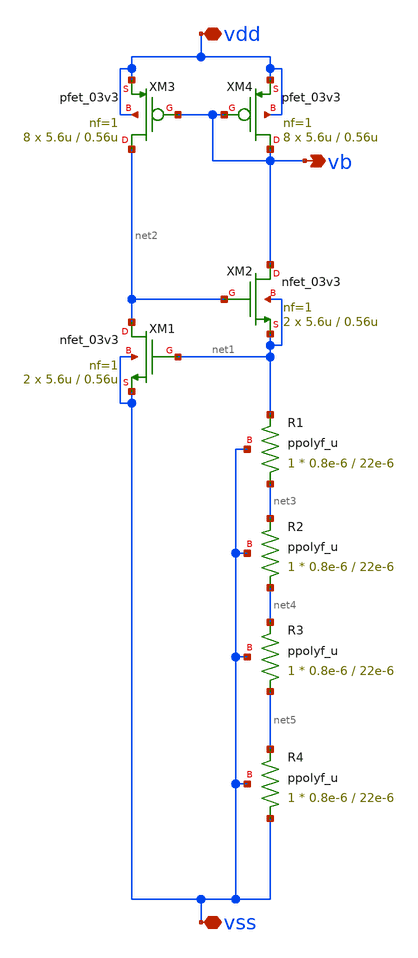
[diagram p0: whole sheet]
** sch_path: noritsuna/ldo/1st_version/cs_vthref.sch
**.subckt cs_vthref vss vdd vb
*.iopin vss
*.iopin vdd
*.opin vb
XM4 vb vb vdd vdd pfet_03v3 L=0.56u W=5.6u nf=1 ad='int((nf+1)/2) * W/nf * 0.18u' as='int((nf+2)/2) * W/nf * 0.18u'
+ pd='2*int((nf+1)/2) * (W/nf + 0.18u)' ps='2*int((nf+2)/2) * (W/nf + 0.18u)' nrd='0.18u / W' nrs='0.18u / W'
+ sa=0 sb=0 sd=0 m=8
XM3 net2 vb vdd vdd pfet_03v3 L=0.56u W=5.6u nf=1 ad='int((nf+1)/2) * W/nf * 0.18u' as='int((nf+2)/2) * W/nf * 0.18u'
+ pd='2*int((nf+1)/2) * (W/nf + 0.18u)' ps='2*int((nf+2)/2) * (W/nf + 0.18u)' nrd='0.18u / W' nrs='0.18u / W'
+ sa=0 sb=0 sd=0 m=8
XM2 vb net2 net1 net1 nfet_03v3 L=0.56u W=5.6u nf=1 ad='int((nf+1)/2) * W/nf * 0.18u' as='int((nf+2)/2) * W/nf * 0.18u'
+ pd='2*int((nf+1)/2) * (W/nf + 0.18u)' ps='2*int((nf+2)/2) * (W/nf + 0.18u)' nrd='0.18u / W' nrs='0.18u / W'
+ sa=0 sb=0 sd=0 m=2
XM1 net2 net1 vss vss nfet_03v3 L=0.56u W=5.6u nf=1 ad='int((nf+1)/2) * W/nf * 0.18u' as='int((nf+2)/2) * W/nf * 0.18u'
+ pd='2*int((nf+1)/2) * (W/nf + 0.18u)' ps='2*int((nf+2)/2) * (W/nf + 0.18u)' nrd='0.18u / W' nrs='0.18u / W'
+ sa=0 sb=0 sd=0 m=2
XR3 net5 net4 vss ppolyf_u r_width=0.8e-6 r_length=22e-6 m=1
XR4 vss net5 vss ppolyf_u r_width=0.8e-6 r_length=22e-6 m=1
XR1 net3 net1 vss ppolyf_u r_width=0.8e-6 r_length=22e-6 m=1
XR2 net4 net3 vss ppolyf_u r_width=0.8e-6 r_length=22e-6 m=1
**.ends
.end
